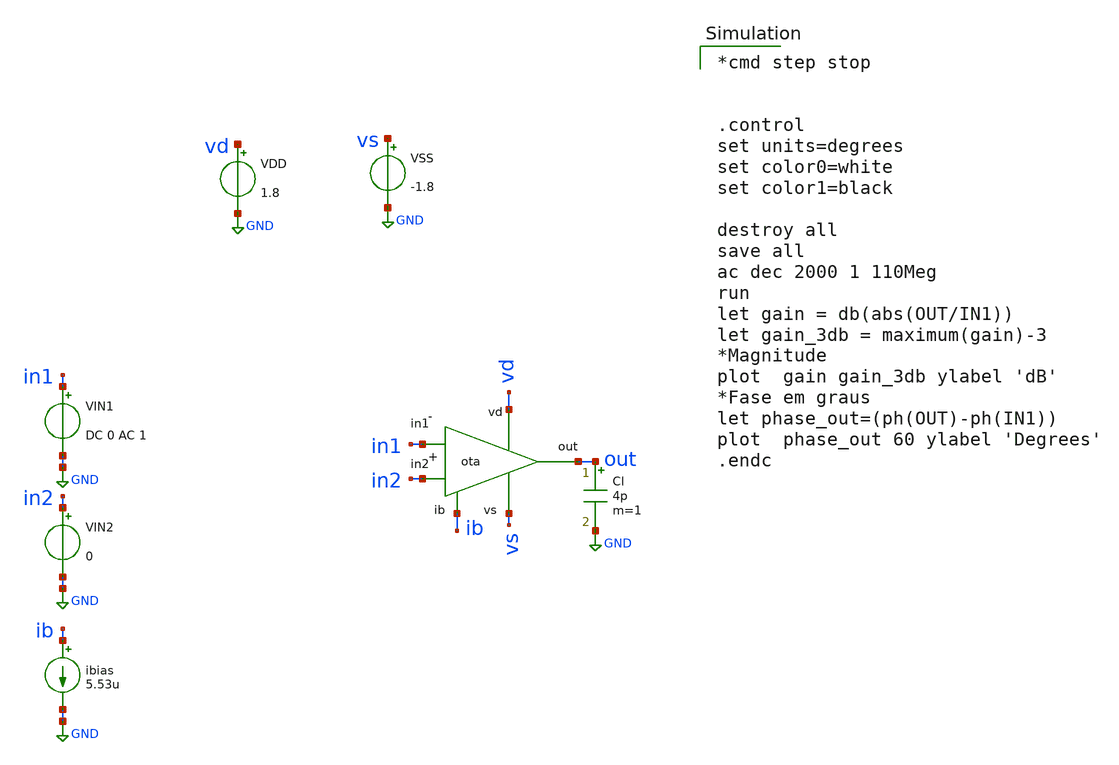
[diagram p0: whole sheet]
** sch_path: amp-op/xschem/ota_tb-ac.sch
* Copyright 2020 Stefan Frederik Schippers
* Licensed under the Apache License, Version 2.0 (the "License");
* you may not use this file except in compliance with the License.
* You may obtain a copy of the License at
* https://www.apache.org/licenses/LICENSE-2.0
* Unless required by applicable law or agreed to in writing, software
* distributed under the License is distributed on an "AS IS" BASIS,
* WITHOUT WARRANTIES OR CONDITIONS OF ANY KIND, either express or implied.
* See the License for the specific language governing permissions and
* limitations under the License.
**.subckt ota_tb-ac
VIN2 in2 GND 0
VIN1 in1 GND DC 0 AC 1
ibias ib GND 5.53u
VDD vd GND 1.8
VSS vs GND -1.8
Cl out GND 4p m=1
X1 vd ib out in2 in1 vs ota
**** begin user architecture code

*cmd step stop


.control
set units=degrees
set color0=white
set color1=black

destroy all
save all
ac dec 2000 1 110Meg
run
let gain = db(abs(OUT/IN1))
let gain_3db = maximum(gain)-3
*Magnitude
plot  gain gain_3db ylabel 'dB'
*Fase em graus
let phase_out=(ph(OUT)-ph(IN1))
plot  phase_out 60 ylabel 'Degrees'
.endc

 .lib $::SKYWATER_MODELS/sky130.lib.spice tt
.include $::SKYWATER_STDCELLS/sky130_fd_sc_hd.spice

**** end user architecture code
**.ends

* expanding   symbol:  /home/hugodg/projects-sky130/temp-sensor/amp-op/xschem/ota.sym # of pins=6
** sym_path: amp-op/xschem/ota.sym
** sch_path: amp-op/xschem/ota.sch
.subckt ota vd ib out in2 in1 vs
*.iopin vd
*.iopin vs
*.iopin ib
*.ipin in1
*.ipin in2
*.opin out
XCC out d sky130_fd_pr__cap_mim_m3_1 W=21 L=21 MF=1 m=1
XM5 ib ib vd vd sky130_fd_pr__pfet_01v8 L=1 W=6 nf=1 ad='int((nf+1)/2) * W/nf * 0.29' as='int((nf+2)/2) * W/nf * 0.29'
+ pd='2*int((nf+1)/2) * (W/nf + 0.29)' ps='2*int((nf+2)/2) * (W/nf + 0.29)' nrd='0.29 / W' nrs='0.29 / W'
+ sa=0 sb=0 sd=0 mult=1 m=1
XM6 b ib vd vd sky130_fd_pr__pfet_01v8 L=1 W=6 nf=1 ad='int((nf+1)/2) * W/nf * 0.29' as='int((nf+2)/2) * W/nf * 0.29'
+ pd='2*int((nf+1)/2) * (W/nf + 0.29)' ps='2*int((nf+2)/2) * (W/nf + 0.29)' nrd='0.29 / W' nrs='0.29 / W'
+ sa=0 sb=0 sd=0 mult=1 m=1
XM8 out ib vd vd sky130_fd_pr__pfet_01v8 L=1 W=30 nf=4 ad='int((nf+1)/2) * W/nf * 0.29' as='int((nf+2)/2) * W/nf * 0.29'
+ pd='2*int((nf+1)/2) * (W/nf + 0.29)' ps='2*int((nf+2)/2) * (W/nf + 0.29)' nrd='0.29 / W' nrs='0.29 / W'
+ sa=0 sb=0 sd=0 mult=1 m=1
XM1 c in1 b b sky130_fd_pr__pfet_01v8 L=1 W=3 nf=1 ad='int((nf+1)/2) * W/nf * 0.29' as='int((nf+2)/2) * W/nf * 0.29'
+ pd='2*int((nf+1)/2) * (W/nf + 0.29)' ps='2*int((nf+2)/2) * (W/nf + 0.29)' nrd='0.29 / W' nrs='0.29 / W'
+ sa=0 sb=0 sd=0 mult=1 m=1
XM2 d in2 b b sky130_fd_pr__pfet_01v8 L=1 W=3 nf=1 ad='int((nf+1)/2) * W/nf * 0.29' as='int((nf+2)/2) * W/nf * 0.29'
+ pd='2*int((nf+1)/2) * (W/nf + 0.29)' ps='2*int((nf+2)/2) * (W/nf + 0.29)' nrd='0.29 / W' nrs='0.29 / W'
+ sa=0 sb=0 sd=0 mult=1 m=1
XM3 c c vs vs sky130_fd_pr__nfet_01v8 L=1 W=1 nf=1 ad='int((nf+1)/2) * W/nf * 0.29' as='int((nf+2)/2) * W/nf * 0.29'
+ pd='2*int((nf+1)/2) * (W/nf + 0.29)' ps='2*int((nf+2)/2) * (W/nf + 0.29)' nrd='0.29 / W' nrs='0.29 / W'
+ sa=0 sb=0 sd=0 mult=1 m=1
XM4 d c vs vs sky130_fd_pr__nfet_01v8 L=1 W=1 nf=1 ad='int((nf+1)/2) * W/nf * 0.29' as='int((nf+2)/2) * W/nf * 0.29'
+ pd='2*int((nf+1)/2) * (W/nf + 0.29)' ps='2*int((nf+2)/2) * (W/nf + 0.29)' nrd='0.29 / W' nrs='0.29 / W'
+ sa=0 sb=0 sd=0 mult=1 m=1
XM7 out d vs vs sky130_fd_pr__nfet_01v8 L=1 W=9 nf=2 ad='int((nf+1)/2) * W/nf * 0.29' as='int((nf+2)/2) * W/nf * 0.29'
+ pd='2*int((nf+1)/2) * (W/nf + 0.29)' ps='2*int((nf+2)/2) * (W/nf + 0.29)' nrd='0.29 / W' nrs='0.29 / W'
+ sa=0 sb=0 sd=0 mult=1 m=1
.ends

.GLOBAL GND
.end
